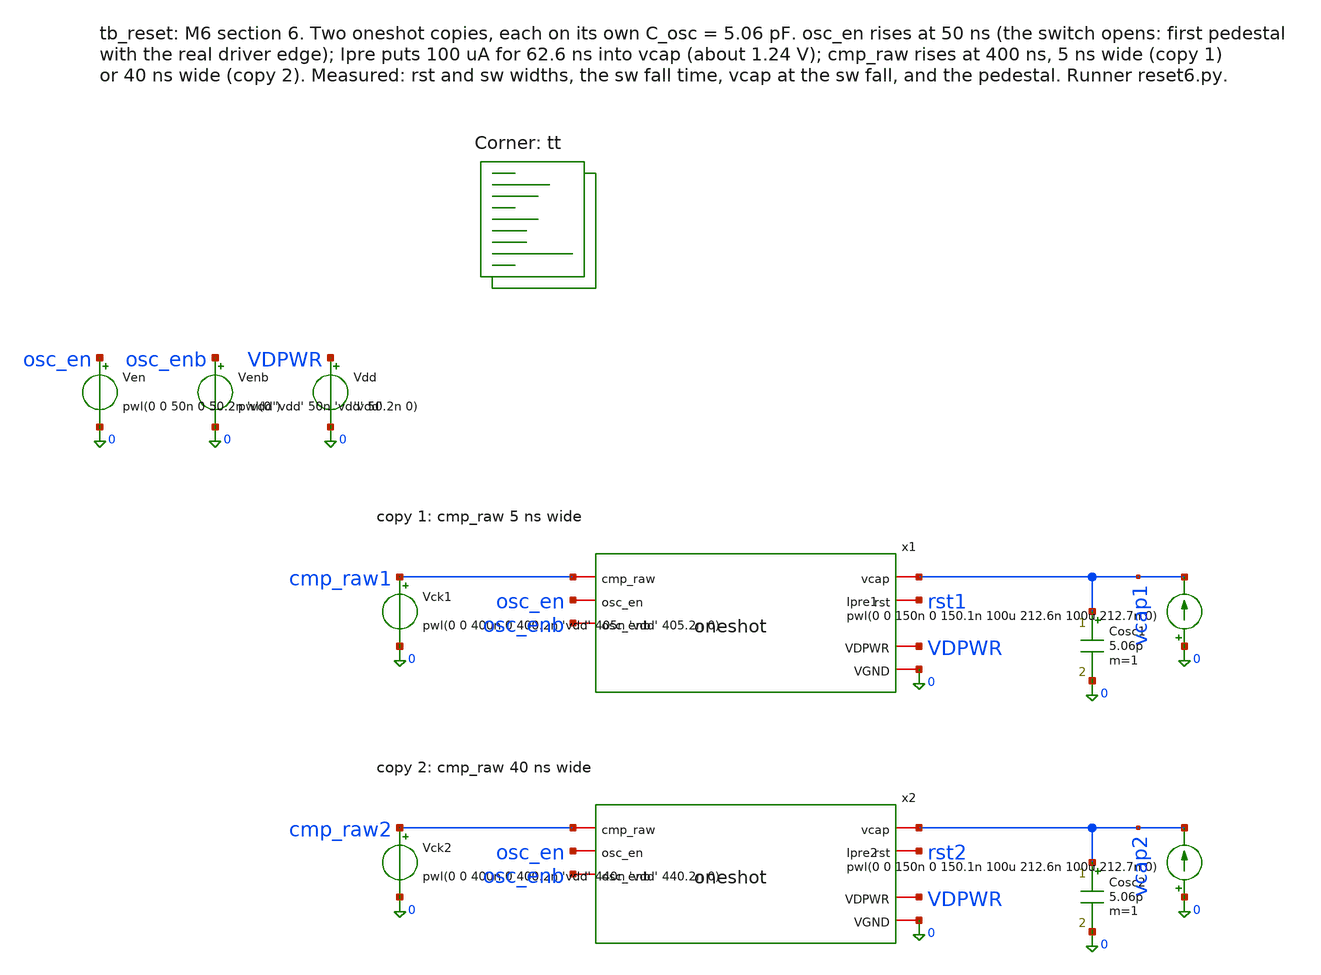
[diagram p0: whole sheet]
** sch_path: xschem/tb_reset.sch
**.subckt tb_reset
x1 cmp_raw1 osc_en osc_enb vcap1 rst1 VDPWR 0 oneshot
Vck1 cmp_raw1 0 pwl(0 0 400n 0 400.2n 'vdd' 405n 'vdd' 405.2n 0)
Cosc1 vcap1 0 5.06p m=1
Ipre1 0 vcap1 pwl(0 0 150n 0 150.1n 100u 212.6n 100u 212.7n 0)
x2 cmp_raw2 osc_en osc_enb vcap2 rst2 VDPWR 0 oneshot
Vck2 cmp_raw2 0 pwl(0 0 400n 0 400.2n 'vdd' 440n 'vdd' 440.2n 0)
Cosc2 vcap2 0 5.06p m=1
Ipre2 0 vcap2 pwl(0 0 150n 0 150.1n 100u 212.6n 100u 212.7n 0)
Ven osc_en 0 pwl(0 0 50n 0 50.2n 'vdd')
Venb osc_enb 0 pwl(0 'vdd' 50n 'vdd' 50.2n 0)
Vdd VDPWR 0 'vdd'
**** begin user architecture code

.param vdd=1.8
.include /foss/pdks/sky130A/libs.ref/sky130_fd_sc_hd/spice/sky130_fd_sc_hd.spice
.temp 25
.option method=gear
.control
tran 0.01n 700n 0 0.02n
meas tran trr1 when v(rst1)=0.9 rise=1 td=300n
meas tran trf1 when v(rst1)=0.9 fall=1 td=300n
meas tran tsr1 when v(x1.sw)=0.9 rise=1 td=300n
meas tran tsf1 when v(x1.sw)=0.9 fall=1 td=300n
meas tran t901 when v(x1.sw)=1.62 fall=1 td=300n
meas tran t101 when v(x1.sw)=0.18 fall=1 td=300n
meas tran vpre1 find v(vcap1) at=390n
meas tran vres1 find v(vcap1) when v(x1.sw)=0.9 fall=1 td=300n
meas tran ped01 find v(vcap1) at=140n
meas tran ped1 find v(vcap1) at=650n
meas tran again1 max v(rst1) from=480n to=690n
echo R k=1 trr=$&trr1 trf=$&trf1 tsr=$&tsr1 tsf=$&tsf1 t90=$&t901 t10=$&t101 vpre=$&vpre1
+ vres=$&vres1 ped0=$&ped01 ped=$&ped1 again=$&again1
meas tran trr2 when v(rst2)=0.9 rise=1 td=300n
meas tran trf2 when v(rst2)=0.9 fall=1 td=300n
meas tran tsr2 when v(x2.sw)=0.9 rise=1 td=300n
meas tran tsf2 when v(x2.sw)=0.9 fall=1 td=300n
meas tran t902 when v(x2.sw)=1.62 fall=1 td=300n
meas tran t102 when v(x2.sw)=0.18 fall=1 td=300n
meas tran vpre2 find v(vcap2) at=390n
meas tran vres2 find v(vcap2) when v(x2.sw)=0.9 fall=1 td=300n
meas tran ped02 find v(vcap2) at=140n
meas tran ped2 find v(vcap2) at=650n
meas tran again2 max v(rst2) from=480n to=690n
echo R k=2 trr=$&trr2 trf=$&trf2 tsr=$&tsr2 tsf=$&tsf2 t90=$&t902 t10=$&t102 vpre=$&vpre2
+ vres=$&vres2 ped0=$&ped02 ped=$&ped2 again=$&again2
.endc

.lib $::SKYWATER_MODELS/sky130.lib.spice tt
**** end user architecture code
**.ends

* expanding   symbol:  oneshot.sym # of pins=7
** sym_path: xschem/oneshot.sym
** sch_path: xschem/oneshot.sch
.subckt oneshot cmp_raw osc_en osc_enb vcap rst VDPWR VGND
*.ipin cmp_raw
*.ipin osc_enb
*.ipin osc_en
*.iopin vcap
*.opin rst
*.iopin VDPWR
*.iopin VGND
xbck cmp_raw VGND VGND VDPWR VDPWR ck sky130_fd_sc_hd__buf_2
xff ck VDPWR rb VGND VGND VDPWR VDPWR rst sky130_fd_sc_hd__dfrtp_1
xor rst osc_enb VGND VGND VDPWR VDPWR swp sky130_fd_sc_hd__or2_1
xi1 swp VGND VGND VDPWR VDPWR swn sky130_fd_sc_hd__inv_1
xand db osc_en VGND VGND VDPWR VDPWR rb sky130_fd_sc_hd__and2_1
xdl rst db VDPWR VGND dly5
XMDP sw swn VDPWR VDPWR sky130_fd_pr__pfet_01v8 L=0.15 W=2 nf=1 ad='int((1 + 1)/2) * 2 / 1 * 0.29' as='int((1 + 2)/2) * 2 / 1 * 0.29'
+ pd='2*int((1 + 1)/2) * (2 / 1 + 0.29)' ps='2*int((1 + 2)/2) * (2 / 1 + 0.29)' nrd='0.29 / 2 ' nrs='0.29 / 2 '
+ sa=0 sb=0 sd=0 mult=1 m=1
XMDN sw swn VGND VGND sky130_fd_pr__nfet_01v8 L=1.5 W=0.42 nf=1 ad='int((1 + 1)/2) * 0.42 / 1 * 0.29'
+ as='int((1 + 2)/2) * 0.42 / 1 * 0.29' pd='2*int((1 + 1)/2) * (0.42 / 1 + 0.29)' ps='2*int((1 + 2)/2) * (0.42 / 1 + 0.29)'
+ nrd='0.29 / 0.42 ' nrs='0.29 / 0.42 ' sa=0 sb=0 sd=0 mult=1 m=1
XMRST vcap sw VGND VGND sky130_fd_pr__nfet_01v8 L=0.5 W=6 nf=1 ad='int((1 + 1)/2) * 6 / 1 * 0.29' as='int((1 + 2)/2) * 6 / 1 * 0.29'
+ pd='2*int((1 + 1)/2) * (6 / 1 + 0.29)' ps='2*int((1 + 2)/2) * (6 / 1 + 0.29)' nrd='0.29 / 6 ' nrs='0.29 / 6 '
+ sa=0 sb=0 sd=0 mult=2 m=2
.ends


* expanding   symbol:  dly5.sym # of pins=4
** sym_path: xschem/dly5.sym
** sch_path: xschem/dly5.sch
.subckt dly5 a y VDPWR VGND
*.iopin VDPWR
*.iopin VGND
*.ipin a
*.opin y
XMP1 d1 a VDPWR VDPWR sky130_fd_pr__pfet_01v8 L=2.3 W=1 nf=1 ad='int((1 + 1)/2) * 1 / 1 * 0.29' as='int((1 + 2)/2) * 1 / 1 * 0.29'
+ pd='2*int((1 + 1)/2) * (1 / 1 + 0.29)' ps='2*int((1 + 2)/2) * (1 / 1 + 0.29)' nrd='0.29 / 1 ' nrs='0.29 / 1 '
+ sa=0 sb=0 sd=0 mult=1 m=1
XMN1 d1 a VGND VGND sky130_fd_pr__nfet_01v8 L=2.3 W=0.42 nf=1 ad='int((1 + 1)/2) * 0.42 / 1 * 0.29' as='int((1 + 2)/2) * 0.42 / 1 * 0.29'
+ pd='2*int((1 + 1)/2) * (0.42 / 1 + 0.29)' ps='2*int((1 + 2)/2) * (0.42 / 1 + 0.29)' nrd='0.29 / 0.42 '
+ nrs='0.29 / 0.42 ' sa=0 sb=0 sd=0 mult=1 m=1
XMP2 d2 d1 VDPWR VDPWR sky130_fd_pr__pfet_01v8 L=2.3 W=1 nf=1 ad='int((1 + 1)/2) * 1 / 1 * 0.29' as='int((1 + 2)/2) * 1 / 1 * 0.29'
+ pd='2*int((1 + 1)/2) * (1 / 1 + 0.29)' ps='2*int((1 + 2)/2) * (1 / 1 + 0.29)' nrd='0.29 / 1 ' nrs='0.29 / 1 '
+ sa=0 sb=0 sd=0 mult=1 m=1
XMN2 d2 d1 VGND VGND sky130_fd_pr__nfet_01v8 L=2.3 W=0.42 nf=1 ad='int((1 + 1)/2) * 0.42 / 1 * 0.29'
+ as='int((1 + 2)/2) * 0.42 / 1 * 0.29' pd='2*int((1 + 1)/2) * (0.42 / 1 + 0.29)' ps='2*int((1 + 2)/2) * (0.42 / 1 + 0.29)'
+ nrd='0.29 / 0.42 ' nrs='0.29 / 0.42 ' sa=0 sb=0 sd=0 mult=1 m=1
XMP3 d3 d2 VDPWR VDPWR sky130_fd_pr__pfet_01v8 L=2.3 W=1 nf=1 ad='int((1 + 1)/2) * 1 / 1 * 0.29' as='int((1 + 2)/2) * 1 / 1 * 0.29'
+ pd='2*int((1 + 1)/2) * (1 / 1 + 0.29)' ps='2*int((1 + 2)/2) * (1 / 1 + 0.29)' nrd='0.29 / 1 ' nrs='0.29 / 1 '
+ sa=0 sb=0 sd=0 mult=1 m=1
XMN3 d3 d2 VGND VGND sky130_fd_pr__nfet_01v8 L=2.3 W=0.42 nf=1 ad='int((1 + 1)/2) * 0.42 / 1 * 0.29'
+ as='int((1 + 2)/2) * 0.42 / 1 * 0.29' pd='2*int((1 + 1)/2) * (0.42 / 1 + 0.29)' ps='2*int((1 + 2)/2) * (0.42 / 1 + 0.29)'
+ nrd='0.29 / 0.42 ' nrs='0.29 / 0.42 ' sa=0 sb=0 sd=0 mult=1 m=1
XMP4 d4 d3 VDPWR VDPWR sky130_fd_pr__pfet_01v8 L=2.3 W=1 nf=1 ad='int((1 + 1)/2) * 1 / 1 * 0.29' as='int((1 + 2)/2) * 1 / 1 * 0.29'
+ pd='2*int((1 + 1)/2) * (1 / 1 + 0.29)' ps='2*int((1 + 2)/2) * (1 / 1 + 0.29)' nrd='0.29 / 1 ' nrs='0.29 / 1 '
+ sa=0 sb=0 sd=0 mult=1 m=1
XMN4 d4 d3 VGND VGND sky130_fd_pr__nfet_01v8 L=2.3 W=0.42 nf=1 ad='int((1 + 1)/2) * 0.42 / 1 * 0.29'
+ as='int((1 + 2)/2) * 0.42 / 1 * 0.29' pd='2*int((1 + 1)/2) * (0.42 / 1 + 0.29)' ps='2*int((1 + 2)/2) * (0.42 / 1 + 0.29)'
+ nrd='0.29 / 0.42 ' nrs='0.29 / 0.42 ' sa=0 sb=0 sd=0 mult=1 m=1
XMP5 y d4 VDPWR VDPWR sky130_fd_pr__pfet_01v8 L=2.3 W=1 nf=1 ad='int((1 + 1)/2) * 1 / 1 * 0.29' as='int((1 + 2)/2) * 1 / 1 * 0.29'
+ pd='2*int((1 + 1)/2) * (1 / 1 + 0.29)' ps='2*int((1 + 2)/2) * (1 / 1 + 0.29)' nrd='0.29 / 1 ' nrs='0.29 / 1 '
+ sa=0 sb=0 sd=0 mult=1 m=1
XMN5 y d4 VGND VGND sky130_fd_pr__nfet_01v8 L=2.3 W=0.42 nf=1 ad='int((1 + 1)/2) * 0.42 / 1 * 0.29' as='int((1 + 2)/2) * 0.42 / 1 * 0.29'
+ pd='2*int((1 + 1)/2) * (0.42 / 1 + 0.29)' ps='2*int((1 + 2)/2) * (0.42 / 1 + 0.29)' nrd='0.29 / 0.42 '
+ nrs='0.29 / 0.42 ' sa=0 sb=0 sd=0 mult=1 m=1
.ends

.end
